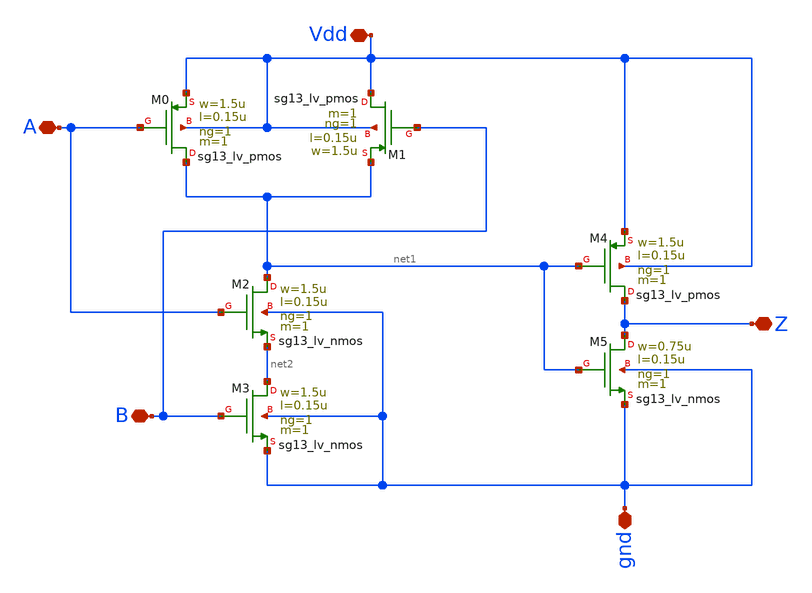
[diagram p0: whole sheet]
** sch_path: design/blocks/and_ms/schematic/and_ms.sch
**.subckt and_ms A B Vdd Z gnd
*.iopin A
*.iopin B
*.iopin Vdd
*.iopin Z
*.iopin gnd
XM2 net1 A net2 gnd sg13_lv_nmos w=1.5u l=0.15u ng=1 m=1 mm_ok=1
XM3 net2 B gnd gnd sg13_lv_nmos w=1.5u l=0.15u ng=1 m=1 mm_ok=1
XM5 Z net1 gnd gnd sg13_lv_nmos w=0.75u l=0.15u ng=1 m=1 mm_ok=1
XM0 net1 A Vdd Vdd sg13_lv_pmos w=1.5u l=0.15u ng=1 m=1 mm_ok=1
XM1 Vdd B net1 Vdd sg13_lv_pmos w=1.5u l=0.15u ng=1 m=1 mm_ok=1
XM4 Z net1 Vdd Vdd sg13_lv_pmos w=1.5u l=0.15u ng=1 m=1 mm_ok=1
**.ends
.end
